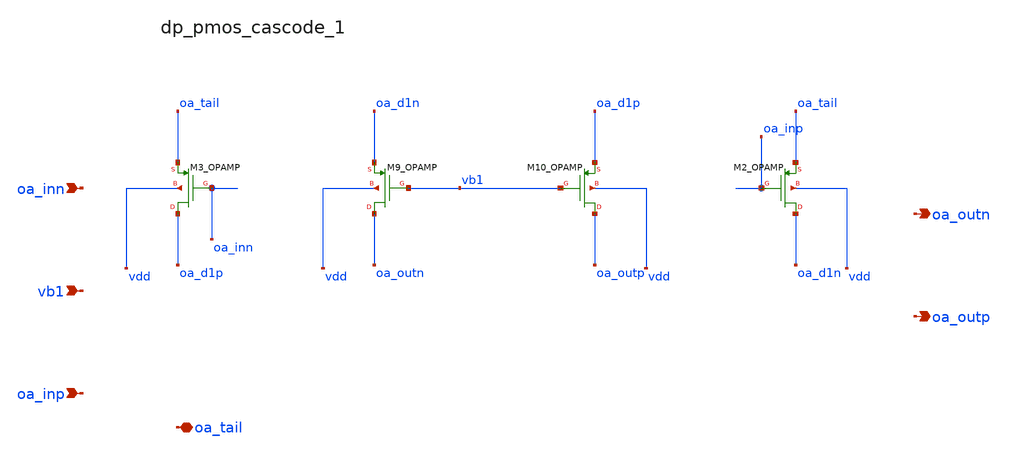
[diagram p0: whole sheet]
** sch_path: analog-db/raw/sup_003_rrl_sc_integrator/hier/blocks/dp_pmos_cascode_1.sch
**.subckt dp_pmos_cascode_1 oa_inn vb1 oa_inp oa_tail oa_outn oa_outp
*.ipin oa_inn
*.ipin vb1
*.ipin oa_inp
*.iopin oa_tail
*.opin oa_outn
*.opin oa_outp
XM10_OPAMP oa_outp vb1 oa_d1p vdd sg13_lv_pmos w=x_dut_xm10_opamp_w l=x_dut_xm10_opamp_l ng=1
+ m=x_dut_xm10_opamp_m
XM2_OPAMP oa_d1n oa_inp oa_tail vdd sg13_lv_pmos w=x_dut_xm2_opamp_w l=x_dut_xm2_opamp_l ng=1
+ m=x_dut_xm2_opamp_m
XM3_OPAMP oa_d1p oa_inn oa_tail vdd sg13_lv_pmos w=x_dut_xm3_opamp_w l=x_dut_xm3_opamp_l ng=1
+ m=x_dut_xm3_opamp_m
XM9_OPAMP oa_outn vb1 oa_d1n vdd sg13_lv_pmos w=x_dut_xm9_opamp_w l=x_dut_xm9_opamp_l ng=1
+ m=x_dut_xm9_opamp_m
**.ends
.end
